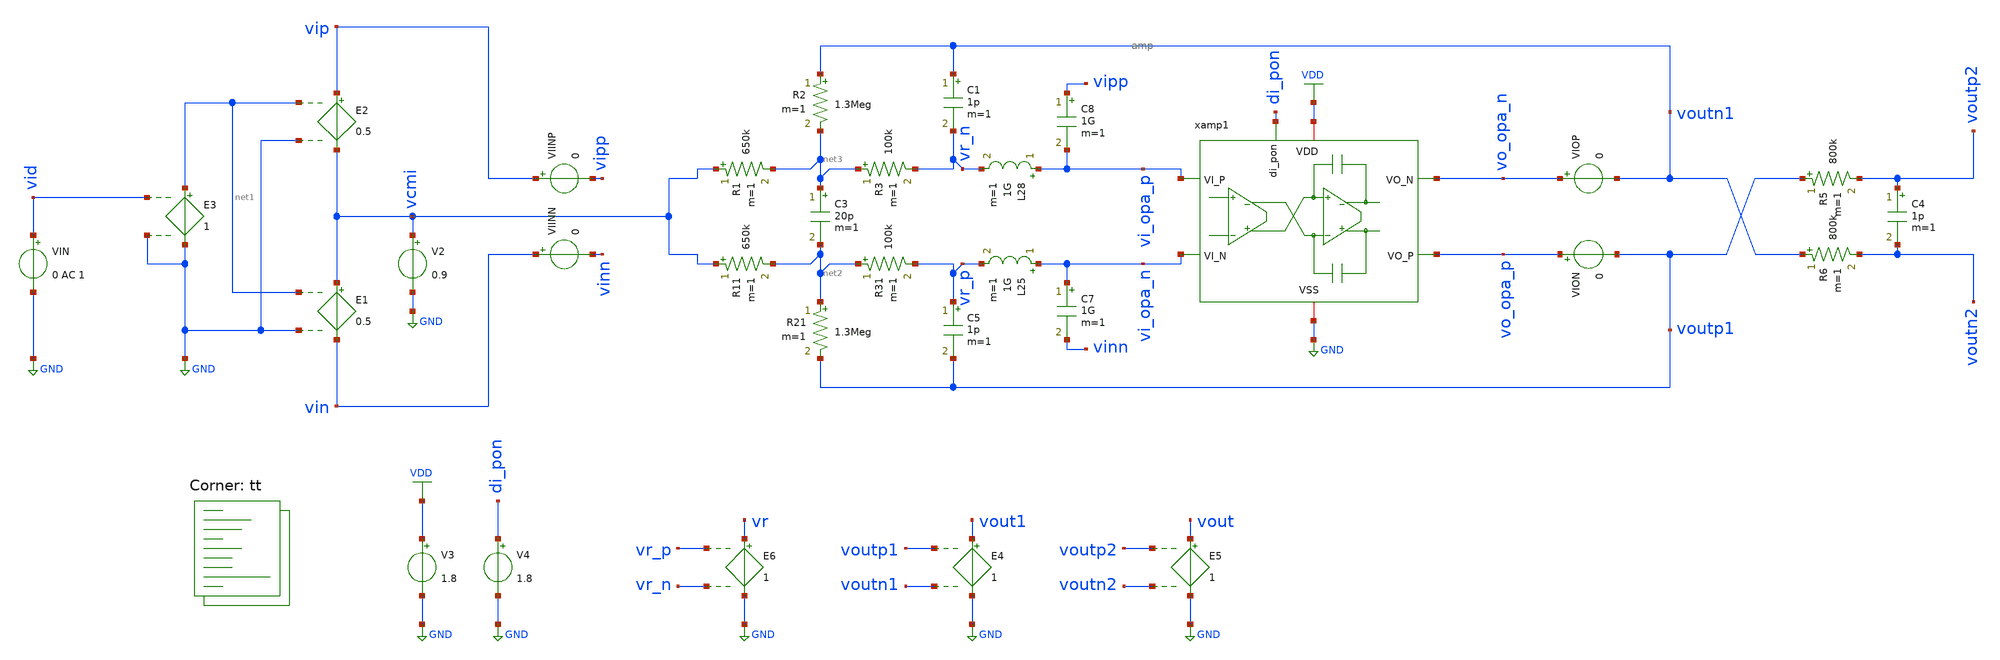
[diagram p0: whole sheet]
** sch_path: xschem/tb_filter_loopgain.sch
**.subckt tb_filter_loopgain
V2 vcmi GND 0.9
E1 vcmi vin net1 GND 0.5
E2 vip vcmi net1 GND 0.5
VIN vid GND 0 AC 1
E3 net1 GND vid GND 1
E4 vout1 GND voutp1 voutn1 1
VIINP vip vipp 0
VIINN vin vinn 0
R1 vcmi net3 650k m=1
R2 voutn1 net3 1.3Meg m=1
R3 net3 vr_n 100k m=1
C1 voutn1 vr_n 1p m=1
C3 net3 net2 20p m=1
R11 vcmi net2 650k m=1
R21 net2 voutp1 1.3Meg m=1
R31 net2 vr_p 100k m=1
C5 vr_p voutp1 1p m=1
E5 vout GND voutp2 voutn2 1
VIOP vo_opa_n voutn1 0
VION vo_opa_p voutp1 0
E6 vr GND vr_p vr_n 1
C7 vi_opa_n vinn 1G m=1
C8 vipp vi_opa_p 1G m=1
L25 vi_opa_n vr_p 1G m=1
L28 vi_opa_p vr_n 1G m=1
xamp1 VDD vi_opa_n vi_opa_p vo_opa_p di_pon vo_opa_n GND amp
V3 VDD GND 1.8
V4 di_pon GND 1.8
C4 voutp2 voutn2 1p m=1
R5 voutp1 voutp2 800k m=1
R6 voutn1 voutn2 800k m=1
**** begin user architecture code
.lib $::SKYWATER_MODELS/sky130.lib.spice tt


*.include /foss/designs/filter/ota_casc_3_dev_save.spice
.options savecurrents
.options method=gear reltol=.01
.options sparse
.control
save all

let f_sig = 100
let f_min = 10
let f_max = 100G
let f_stop = 5Meg
let tper_sig = 1/f_sig
let tfr_sig = tper_sig/2
let Adc = 10
let beta = 1/Adc
let v_step_o = 0.9
let v_step_i = v_step_o/Adc

let t_rf = 0.1u
let t_step = 50u
let t_delay = 0
let t_per = 2*t_step

let tstep = 0.1*t_rf
let tstop = 2*t_per
let tstart = t_delay

*alter @VIN[SIN] = [ 0 0.01 $&f_sig 0 0 0 ]
alter @VIN[DC] = 0.0


*set fndc = /foss/designs/frontend/frontend_dc.txt
*set fntran = /foss/designs/frontend/frontend_tran.txt
*set fnspec = /foss/designs/frontend/frontend_spec.txt
*set fnhd = /foss/designs/frontend/frontend_hd.txt
*set fnnoise = /foss/designs/frontend/frontend_noise.txt
set wr_singlescale
set wr_vecnames
option numdgt=3


** Main Simulations
	op
	ac dec 100 $&const.f_min $&const.f_max

	setplot ac1
	let A1 = v(vout1)/v(vid)
	let A2 = v(vout)/v(vid)
	let L = v(vr)/v(vid)
	let A = L/beta

	let L_re = real(L)
	let L_im = imag(L)

	let L_dB = vdb(L)
	let L_arg = 180/PI*cphase(L)
	let A_dB = vdb(A)
	let A_arg = 180/PI*cphase(A)

	let fdc = const.f_min+1

	meas ac fug find frequency when L_dB=0
	meas ac pm find L_arg when frequency=fug

	let pm = 180-abs(pm)

	print pm

	let err_gain = 1-10^(Adc/20)/10
	let Adc_ol_min = (1-err_gain)/err_gain

	print err_gain
	print Adc_ol_min

	plot L_dB L_arg A_dB A_arg title 'Bode Plot of Loop Gain' ylabel 'Magnitude (dB) / Phase (Deg)'
	plot L_im vs L_re retraceplot title 'Nyquist Plot of Loop Gain' ylabel 'Imaginary Part' xlabel 'Real Part'


alter @VIN[DC] = 0
op

remzerovec
write tb_filter_loopgain.raw
.endc

**** end user architecture code
**.ends

* expanding   symbol:  /foss/designs/xschem/amp.sym # of pins=7
** sym_path: xschem/amp.sym
** sch_path: xschem/amp.sch
.subckt amp VDD VI_N VI_P VO_P di_pon VO_N VSS
*.iopin VSS
*.iopin VDD
*.ipin VI_P
*.ipin di_pon
*.ipin VI_N
*.opin VO_P
*.opin VO_N
XMP1 vbp vbp VDD VDD sky130_fd_pr__pfet_01v8 L=0.25 W='5 * 2 ' nf=2 ad='int((nf+1)/2) * W / nf * 0.29'
+ as='int((nf+2)/2) * W / nf * 0.29' pd='2*int((nf+1)/2) * (W / nf + 0.29)' ps='2*int((nf+2)/2) * (W / nf + 0.29)'
+ nrd='0.29 / W ' nrs='0.29 / W ' sa=0 sb=0 sd=0 mult=1 m=1
XMPSW3 vbp pon VDD VDD sky130_fd_pr__pfet_01v8 L=0.15 W='5 * 5 ' nf=5 ad='int((nf+1)/2) * W / nf * 0.29'
+ as='int((nf+2)/2) * W / nf * 0.29' pd='2*int((nf+1)/2) * (W / nf + 0.29)' ps='2*int((nf+2)/2) * (W / nf + 0.29)'
+ nrd='0.29 / W ' nrs='0.29 / W ' sa=0 sb=0 sd=0 mult=1 m=1
XMNSW1 pon_b di_pon VSS VSS sky130_fd_pr__nfet_01v8 L=0.15 W='3 * 1 ' nf=1 ad='int((nf+1)/2) * W / nf * 0.29'
+ as='int((nf+2)/2) * W / nf * 0.29' pd='2*int((nf+1)/2) * (W / nf + 0.29)' ps='2*int((nf+2)/2) * (W / nf + 0.29)'
+ nrd='0.29 / W ' nrs='0.29 / W ' sa=0 sb=0 sd=0 mult=1 m=1
XMPSW1 pon_b di_pon VDD VDD sky130_fd_pr__pfet_01v8 L=0.15 W='5 * 1 ' nf=1 ad='int((nf+1)/2) * W / nf * 0.29'
+ as='int((nf+2)/2) * W / nf * 0.29' pd='2*int((nf+1)/2) * (W / nf + 0.29)' ps='2*int((nf+2)/2) * (W / nf + 0.29)'
+ nrd='0.29 / W ' nrs='0.29 / W ' sa=0 sb=0 sd=0 mult=1 m=1
XMNSW2 pon pon_b VSS VSS sky130_fd_pr__nfet_01v8 L=0.15 W='3 * 3 ' nf=3 ad='int((nf+1)/2) * W / nf * 0.29'
+ as='int((nf+2)/2) * W / nf * 0.29' pd='2*int((nf+1)/2) * (W / nf + 0.29)' ps='2*int((nf+2)/2) * (W / nf + 0.29)'
+ nrd='0.29 / W ' nrs='0.29 / W ' sa=0 sb=0 sd=0 mult=1 m=1
XMPSW2 pon pon_b VDD VDD sky130_fd_pr__pfet_01v8 L=0.15 W='5 * 3 ' nf=3 ad='int((nf+1)/2) * W / nf * 0.29'
+ as='int((nf+2)/2) * W / nf * 0.29' pd='2*int((nf+1)/2) * (W / nf + 0.29)' ps='2*int((nf+2)/2) * (W / nf + 0.29)'
+ nrd='0.29 / W ' nrs='0.29 / W ' sa=0 sb=0 sd=0 mult=1 m=1
XMP2 viref1 vbp VDD VDD sky130_fd_pr__pfet_01v8 L=0.25 W='5 * 20 ' nf=20 ad='int((nf+1)/2) * W / nf * 0.29'
+ as='int((nf+2)/2) * W / nf * 0.29' pd='2*int((nf+1)/2) * (W / nf + 0.29)' ps='2*int((nf+2)/2) * (W / nf + 0.29)'
+ nrd='0.29 / W ' nrs='0.29 / W ' sa=0 sb=0 sd=0 mult=1 m=1
XC5 VDD vbp sky130_fd_pr__cap_mim_m3_1 W=5 L=5 MF=5 m=5
XMP4 vo1_n VI_P viref1 viref1 sky130_fd_pr__pfet_01v8 L=0.15 W='5 * 70 ' nf=70 ad='int((nf+1)/2) * W / nf * 0.29'
+ as='int((nf+2)/2) * W / nf * 0.29' pd='2*int((nf+1)/2) * (W / nf + 0.29)' ps='2*int((nf+2)/2) * (W / nf + 0.29)'
+ nrd='0.29 / W ' nrs='0.29 / W ' sa=0 sb=0 sd=0 mult=1 m=1
XMP5 vo1_p VI_N viref1 viref1 sky130_fd_pr__pfet_01v8 L=0.15 W='5 * 70 ' nf=70 ad='int((nf+1)/2) * W / nf * 0.29'
+ as='int((nf+2)/2) * W / nf * 0.29' pd='2*int((nf+1)/2) * (W / nf + 0.29)' ps='2*int((nf+2)/2) * (W / nf + 0.29)'
+ nrd='0.29 / W ' nrs='0.29 / W ' sa=0 sb=0 sd=0 mult=1 m=1
XMN1 vo1_n vfb1 VSS VSS sky130_fd_pr__nfet_01v8 L=1 W='3 * 6 ' nf=6 ad='int((nf+1)/2) * W / nf * 0.29'
+ as='int((nf+2)/2) * W / nf * 0.29' pd='2*int((nf+1)/2) * (W / nf + 0.29)' ps='2*int((nf+2)/2) * (W / nf + 0.29)'
+ nrd='0.29 / W ' nrs='0.29 / W ' sa=0 sb=0 sd=0 mult=1 m=1
XMN2 vo1_p vfb1 VSS VSS sky130_fd_pr__nfet_01v8 L=1 W='3 * 6 ' nf=6 ad='int((nf+1)/2) * W / nf * 0.29'
+ as='int((nf+2)/2) * W / nf * 0.29' pd='2*int((nf+1)/2) * (W / nf + 0.29)' ps='2*int((nf+2)/2) * (W / nf + 0.29)'
+ nrd='0.29 / W ' nrs='0.29 / W ' sa=0 sb=0 sd=0 mult=1 m=1
XC1 vo1_n vfb1 sky130_fd_pr__cap_mim_m3_1 W=5 L=5 MF=5 m=5
XC2 vfb1 vo1_p sky130_fd_pr__cap_mim_m3_1 W=5 L=5 MF=5 m=5
XMN3 VO_N vo1_p VSS VSS sky130_fd_pr__nfet_01v8 L=0.5 W='3 * 20 ' nf=20 ad='int((nf+1)/2) * W / nf * 0.29'
+ as='int((nf+2)/2) * W / nf * 0.29' pd='2*int((nf+1)/2) * (W / nf + 0.29)' ps='2*int((nf+2)/2) * (W / nf + 0.29)'
+ nrd='0.29 / W ' nrs='0.29 / W ' sa=0 sb=0 sd=0 mult=1 m=1
XMN4 VO_P vo1_n VSS VSS sky130_fd_pr__nfet_01v8 L=0.5 W='3 * 20 ' nf=20 ad='int((nf+1)/2) * W / nf * 0.29'
+ as='int((nf+2)/2) * W / nf * 0.29' pd='2*int((nf+1)/2) * (W / nf + 0.29)' ps='2*int((nf+2)/2) * (W / nf + 0.29)'
+ nrd='0.29 / W ' nrs='0.29 / W ' sa=0 sb=0 sd=0 mult=1 m=1
XMP3 vbncm vbp VDD VDD sky130_fd_pr__pfet_01v8 L=0.25 W='5 * 2 ' nf=2 ad='int((nf+1)/2) * W / nf * 0.29'
+ as='int((nf+2)/2) * W / nf * 0.29' pd='2*int((nf+1)/2) * (W / nf + 0.29)' ps='2*int((nf+2)/2) * (W / nf + 0.29)'
+ nrd='0.29 / W ' nrs='0.29 / W ' sa=0 sb=0 sd=0 mult=1 m=1
XMP6 VO_P vfb2 VDD VDD sky130_fd_pr__pfet_01v8 L=0.5 W='5 * 5 ' nf=5 ad='int((nf+1)/2) * W / nf * 0.29'
+ as='int((nf+2)/2) * W / nf * 0.29' pd='2*int((nf+1)/2) * (W / nf + 0.29)' ps='2*int((nf+2)/2) * (W / nf + 0.29)'
+ nrd='0.29 / W ' nrs='0.29 / W ' sa=0 sb=0 sd=0 mult=1 m=1
XMP7 VO_N vfb2 VDD VDD sky130_fd_pr__pfet_01v8 L=0.5 W='5 * 5 ' nf=5 ad='int((nf+1)/2) * W / nf * 0.29'
+ as='int((nf+2)/2) * W / nf * 0.29' pd='2*int((nf+1)/2) * (W / nf + 0.29)' ps='2*int((nf+2)/2) * (W / nf + 0.29)'
+ nrd='0.29 / W ' nrs='0.29 / W ' sa=0 sb=0 sd=0 mult=1 m=1
XC3 VO_N vfb2 sky130_fd_pr__cap_mim_m3_1 W=5 L=5 MF=5 m=5
XC4 vfb2 VO_P sky130_fd_pr__cap_mim_m3_1 W=5 L=5 MF=5 m=5
XMN5 vbncm vbncm VSS VSS sky130_fd_pr__nfet_01v8 L=0.5 W='3 * 5 ' nf=5 ad='int((nf+1)/2) * W / nf * 0.29'
+ as='int((nf+2)/2) * W / nf * 0.29' pd='2*int((nf+1)/2) * (W / nf + 0.29)' ps='2*int((nf+2)/2) * (W / nf + 0.29)'
+ nrd='0.29 / W ' nrs='0.29 / W ' sa=0 sb=0 sd=0 mult=1 m=1
XMN6 vfb2 vbncm VSS VSS sky130_fd_pr__nfet_01v8 L=0.5 W='3 * 4 ' nf=4 ad='int((nf+1)/2) * W / nf * 0.29'
+ as='int((nf+2)/2) * W / nf * 0.29' pd='2*int((nf+1)/2) * (W / nf + 0.29)' ps='2*int((nf+2)/2) * (W / nf + 0.29)'
+ nrd='0.29 / W ' nrs='0.29 / W ' sa=0 sb=0 sd=0 mult=1 m=1
XMNSW3 vrref_sw pon VSS VSS sky130_fd_pr__nfet_01v8 L=0.15 W='3 * 5 ' nf=5 ad='int((nf+1)/2) * W / nf * 0.29'
+ as='int((nf+2)/2) * W / nf * 0.29' pd='2*int((nf+1)/2) * (W / nf + 0.29)' ps='2*int((nf+2)/2) * (W / nf + 0.29)'
+ nrd='0.29 / W ' nrs='0.29 / W ' sa=0 sb=0 sd=0 mult=1 m=1
XRREF vrref_sw vbp VSS sky130_fd_pr__res_xhigh_po_0p35 L=5.6 mult=1 m=1
xr1 vfb1 vo1_n vo1_p VSS rstring_cm
xr2 vfb2 VO_P VO_N VSS rstring_cm
XC6 vo1_p VO_N sky130_fd_pr__cap_mim_m3_1 W=5 L=5 MF=16 m=16
XC7 vo1_n VO_P sky130_fd_pr__cap_mim_m3_1 W=5 L=5 MF=16 m=16
.ends


* expanding   symbol:  /foss/designs/xschem/rstring_cm.sym # of pins=4
** sym_path: xschem/rstring_cm.sym
** sch_path: xschem/rstring_cm.sch
.subckt rstring_cm VR_M VR_N VR_P VSS
*.iopin VSS
*.ipin VR_P
*.ipin VR_N
*.opin VR_M
XR1 VR_P net1 VSS sky130_fd_pr__res_xhigh_po_0p35 L=5.6 mult=1 m=1
XR2 net1 VR_M VSS sky130_fd_pr__res_xhigh_po_0p35 L=5.6 mult=1 m=1
XR3 VR_M net2 VSS sky130_fd_pr__res_xhigh_po_0p35 L=5.6 mult=1 m=1
XR4 net2 VR_N VSS sky130_fd_pr__res_xhigh_po_0p35 L=5.6 mult=1 m=1
.ends

.GLOBAL GND
.GLOBAL VDD
.end
